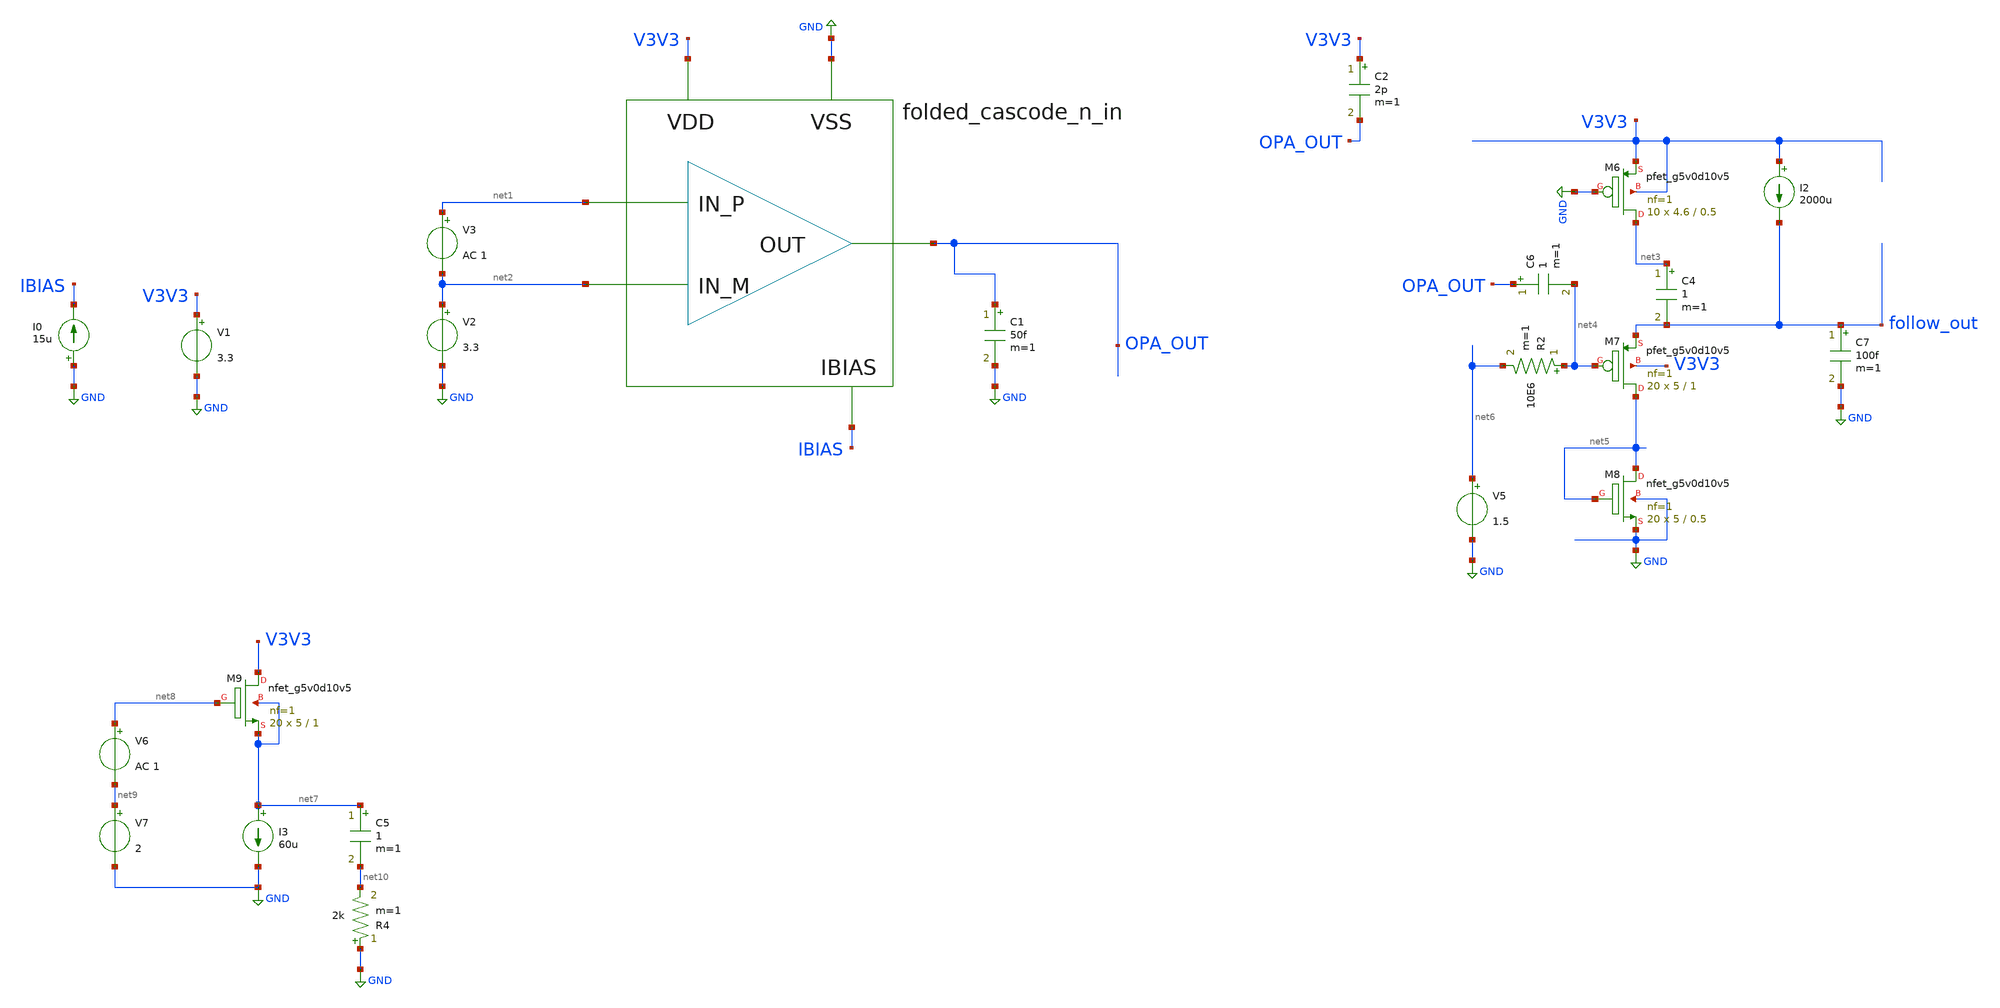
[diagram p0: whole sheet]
** sch_path: design/current-sense/current_sense_ac_bode.sch
**.subckt current_sense_ac_bode
V1 V3V3 GND 3.3
I0 GND IBIAS 15u
x1 net1 net2 OPA_OUT V3V3 GND IBIAS folded_cascode_n_in
C1 OPA_OUT GND 50f m=1
V2 net2 GND 3.3
V3 net1 net2 AC 1
XM6 net3 GND V3V3 V3V3 sky130_fd_pr__pfet_g5v0d10v5 L=0.5 W=4.6 nf=1 ad='int((nf+1)/2) * W/nf * 0.29'
+ as='int((nf+2)/2) * W/nf * 0.29' pd='2*int((nf+1)/2) * (W/nf + 0.29)' ps='2*int((nf+2)/2) * (W/nf + 0.29)'
+ nrd='0.29 / W' nrs='0.29 / W' sa=0 sb=0 sd=0 mult=10 m=10
XM7 net5 net4 follow_out V3V3 sky130_fd_pr__pfet_g5v0d10v5 L=1 W=5 nf=1 ad='int((nf+1)/2) * W/nf * 0.29'
+ as='int((nf+2)/2) * W/nf * 0.29' pd='2*int((nf+1)/2) * (W/nf + 0.29)' ps='2*int((nf+2)/2) * (W/nf + 0.29)'
+ nrd='0.29 / W' nrs='0.29 / W' sa=0 sb=0 sd=0 mult=20 m=20
I2 V3V3 follow_out 2000u
XM8 net5 net5 GND GND sky130_fd_pr__nfet_g5v0d10v5 L=0.5 W=5 nf=1 ad='int((nf+1)/2) * W/nf * 0.29' as='int((nf+2)/2) * W/nf * 0.29'
+ pd='2*int((nf+1)/2) * (W/nf + 0.29)' ps='2*int((nf+2)/2) * (W/nf + 0.29)' nrd='0.29 / W' nrs='0.29 / W'
+ sa=0 sb=0 sd=0 mult=20 m=20
V5 net6 GND 1.5
C4 net3 follow_out 1 m=1
XM9 V3V3 net8 net7 net7 sky130_fd_pr__nfet_g5v0d10v5 L=1 W=5 nf=1 ad='int((nf+1)/2) * W/nf * 0.29' as='int((nf+2)/2) * W/nf * 0.29'
+ pd='2*int((nf+1)/2) * (W/nf + 0.29)' ps='2*int((nf+2)/2) * (W/nf + 0.29)' nrd='0.29 / W' nrs='0.29 / W'
+ sa=0 sb=0 sd=0 mult=20 m=20
I3 net7 GND 60u
V6 net8 net9 AC 1
V7 net9 GND 2
R2 net4 net6 10E6 m=1
C5 net7 net10 1 m=1
R4 GND net10 2k m=1
C6 OPA_OUT net4 1 m=1
C7 follow_out GND 100f m=1
C2 V3V3 OPA_OUT 2p m=1
**** begin user architecture code



.control
.save all
.options savecurrents
ac dec 200 10 1000Meg
settype decibel opa_out
plot vdb(opa_out)
let opa_outd = 180/PI*cph(opa_out)
settype phase opa_outd
plot opa_outd

settype decibel follow_out
plot vdb(follow_out)
let follow_outd = 180/PI*cph(follow_out)
settype phase follow_outd
plot follow_outd
write current_sense_ac.raw
.endc



.lib $::SKYWATER_MODELS/models/sky130.lib.spice ss

**** end user architecture code
**.ends

* expanding   symbol:  design/folded-cascode-n-in/folded_cascode_n_in.sym # of pins=6
** sym_path: design/folded-cascode-n-in/folded_cascode_n_in.sym
** sch_path: design/folded-cascode-n-in/folded_cascode_n_in.sch
.subckt folded_cascode_n_in IN_P IN_M OUT VDD VSS VBN
*.ipin IN_P
*.ipin IN_M
*.ipin OUT
*.ipin VDD
*.ipin VSS
*.ipin VBN
XM1 net1 VBN VSS VSS sky130_fd_pr__nfet_g5v0d10v5 L=1 W=5 nf=1 ad='int((nf+1)/2) * W/nf * 0.29' as='int((nf+2)/2) * W/nf * 0.29'
+ pd='2*int((nf+1)/2) * (W/nf + 0.29)' ps='2*int((nf+2)/2) * (W/nf + 0.29)' nrd='0.29 / W' nrs='0.29 / W'
+ sa=0 sb=0 sd=0 mult=12 m=12
XM3 VS1_P IN_M net1 VSS sky130_fd_pr__nfet_g5v0d10v5 L=1 W=5 nf=1 ad='int((nf+1)/2) * W/nf * 0.29' as='int((nf+2)/2) * W/nf * 0.29'
+ pd='2*int((nf+1)/2) * (W/nf + 0.29)' ps='2*int((nf+2)/2) * (W/nf + 0.29)' nrd='0.29 / W' nrs='0.29 / W'
+ sa=0 sb=0 sd=0 mult=24 m=24
XM4 VS1_M IN_P net1 VSS sky130_fd_pr__nfet_g5v0d10v5 L=1 W=5 nf=1 ad='int((nf+1)/2) * W/nf * 0.29' as='int((nf+2)/2) * W/nf * 0.29'
+ pd='2*int((nf+1)/2) * (W/nf + 0.29)' ps='2*int((nf+2)/2) * (W/nf + 0.29)' nrd='0.29 / W' nrs='0.29 / W'
+ sa=0 sb=0 sd=0 mult=24 m=24
XM9 net2 VCN net4 VSS sky130_fd_pr__nfet_g5v0d10v5 L=1 W=5 nf=1 ad='int((nf+1)/2) * W/nf * 0.29' as='int((nf+2)/2) * W/nf * 0.29'
+ pd='2*int((nf+1)/2) * (W/nf + 0.29)' ps='2*int((nf+2)/2) * (W/nf + 0.29)' nrd='0.29 / W' nrs='0.29 / W'
+ sa=0 sb=0 sd=0 mult=4 m=4
XM10 net3 net2 VSS VSS sky130_fd_pr__nfet_g5v0d10v5 L=1 W=5 nf=1 ad='int((nf+1)/2) * W/nf * 0.29' as='int((nf+2)/2) * W/nf * 0.29'
+ pd='2*int((nf+1)/2) * (W/nf + 0.29)' ps='2*int((nf+2)/2) * (W/nf + 0.29)' nrd='0.29 / W' nrs='0.29 / W'
+ sa=0 sb=0 sd=0 mult=4 m=4
XM11 net4 net2 VSS VSS sky130_fd_pr__nfet_g5v0d10v5 L=1 W=5 nf=1 ad='int((nf+1)/2) * W/nf * 0.29' as='int((nf+2)/2) * W/nf * 0.29'
+ pd='2*int((nf+1)/2) * (W/nf + 0.29)' ps='2*int((nf+2)/2) * (W/nf + 0.29)' nrd='0.29 / W' nrs='0.29 / W'
+ sa=0 sb=0 sd=0 mult=4 m=4
XM12 OUT VCN net3 VSS sky130_fd_pr__nfet_g5v0d10v5 L=1 W=5 nf=1 ad='int((nf+1)/2) * W/nf * 0.29' as='int((nf+2)/2) * W/nf * 0.29'
+ pd='2*int((nf+1)/2) * (W/nf + 0.29)' ps='2*int((nf+2)/2) * (W/nf + 0.29)' nrd='0.29 / W' nrs='0.29 / W'
+ sa=0 sb=0 sd=0 mult=4 m=4
XM5 VS1_P VBP_INT VDD VDD sky130_fd_pr__pfet_g5v0d10v5 L=1 W=5 nf=1 ad='int((nf+1)/2) * W/nf * 0.29'
+ as='int((nf+2)/2) * W/nf * 0.29' pd='2*int((nf+1)/2) * (W/nf + 0.29)' ps='2*int((nf+2)/2) * (W/nf + 0.29)'
+ nrd='0.29 / W' nrs='0.29 / W' sa=0 sb=0 sd=0 mult=10 m=10
XM13 VS1_M VBP_INT VDD VDD sky130_fd_pr__pfet_g5v0d10v5 L=1 W=5 nf=1 ad='int((nf+1)/2) * W/nf * 0.29'
+ as='int((nf+2)/2) * W/nf * 0.29' pd='2*int((nf+1)/2) * (W/nf + 0.29)' ps='2*int((nf+2)/2) * (W/nf + 0.29)'
+ nrd='0.29 / W' nrs='0.29 / W' sa=0 sb=0 sd=0 mult=10 m=10
XM17 VBP_INT VBN VSS VSS sky130_fd_pr__nfet_g5v0d10v5 L=1 W=5 nf=1 ad='int((nf+1)/2) * W/nf * 0.29' as='int((nf+2)/2) * W/nf * 0.29'
+ pd='2*int((nf+1)/2) * (W/nf + 0.29)' ps='2*int((nf+2)/2) * (W/nf + 0.29)' nrd='0.29 / W' nrs='0.29 / W'
+ sa=0 sb=0 sd=0 mult=1 m=1
XM18 VBP_INT VBP_INT VDD VDD sky130_fd_pr__pfet_g5v0d10v5 L=1 W=5 nf=1 ad='int((nf+1)/2) * W/nf * 0.29'
+ as='int((nf+2)/2) * W/nf * 0.29' pd='2*int((nf+1)/2) * (W/nf + 0.29)' ps='2*int((nf+2)/2) * (W/nf + 0.29)'
+ nrd='0.29 / W' nrs='0.29 / W' sa=0 sb=0 sd=0 mult=1 m=1
XM14 net2 VCP VS1_M VDD sky130_fd_pr__pfet_g5v0d10v5 L=1 W=5 nf=1 ad='int((nf+1)/2) * W/nf * 0.29' as='int((nf+2)/2) * W/nf * 0.29'
+ pd='2*int((nf+1)/2) * (W/nf + 0.29)' ps='2*int((nf+2)/2) * (W/nf + 0.29)' nrd='0.29 / W' nrs='0.29 / W'
+ sa=0 sb=0 sd=0 mult=4 m=4
XM19 OUT VCP VS1_P VDD sky130_fd_pr__pfet_g5v0d10v5 L=1 W=5 nf=1 ad='int((nf+1)/2) * W/nf * 0.29' as='int((nf+2)/2) * W/nf * 0.29'
+ pd='2*int((nf+1)/2) * (W/nf + 0.29)' ps='2*int((nf+2)/2) * (W/nf + 0.29)' nrd='0.29 / W' nrs='0.29 / W'
+ sa=0 sb=0 sd=0 mult=4 m=4
XM2 VBP_INT VBP_INT VS1_P VSS sky130_fd_pr__nfet_g5v0d10v5 L=1 W=5 nf=1 ad='int((nf+1)/2) * W/nf * 0.29'
+ as='int((nf+2)/2) * W/nf * 0.29' pd='2*int((nf+1)/2) * (W/nf + 0.29)' ps='2*int((nf+2)/2) * (W/nf + 0.29)'
+ nrd='0.29 / W' nrs='0.29 / W' sa=0 sb=0 sd=0 mult=1 m=1
XM6 VBP_INT VBP_INT VS1_M VSS sky130_fd_pr__nfet_g5v0d10v5 L=1 W=5 nf=1 ad='int((nf+1)/2) * W/nf * 0.29'
+ as='int((nf+2)/2) * W/nf * 0.29' pd='2*int((nf+1)/2) * (W/nf + 0.29)' ps='2*int((nf+2)/2) * (W/nf + 0.29)'
+ nrd='0.29 / W' nrs='0.29 / W' sa=0 sb=0 sd=0 mult=1 m=1
x1 VBN VCN net5 VCP VDD VSS cascode_bias
.ends


* expanding   symbol:  design/bias-circuit/cascode_bias.sym # of pins=6
** sym_path: design/bias-circuit/cascode_bias.sym
** sch_path: design/bias-circuit/cascode_bias.sch
.subckt cascode_bias VBN VCN VBP VCP VDD VSS
*.ipin VCN
*.ipin VBP
*.ipin VCP
*.ipin VDD
*.ipin VSS
*.ipin VBN
XM1 VBP VBP VDD VDD sky130_fd_pr__pfet_g5v0d10v5 L=1 W=5 nf=1 ad='int((nf+1)/2) * W/nf * 0.29' as='int((nf+2)/2) * W/nf * 0.29'
+ pd='2*int((nf+1)/2) * (W/nf + 0.29)' ps='2*int((nf+2)/2) * (W/nf + 0.29)' nrd='0.29 / W' nrs='0.29 / W'
+ sa=0 sb=0 sd=0 mult=1 m=1
XM2 net1 VBP net8 VDD sky130_fd_pr__pfet_g5v0d10v5 L=1 W=5 nf=1 ad='int((nf+1)/2) * W/nf * 0.29' as='int((nf+2)/2) * W/nf * 0.29'
+ pd='2*int((nf+1)/2) * (W/nf + 0.29)' ps='2*int((nf+2)/2) * (W/nf + 0.29)' nrd='0.29 / W' nrs='0.29 / W'
+ sa=0 sb=0 sd=0 mult=1 m=1
XM3 VCN VBP VDD VDD sky130_fd_pr__pfet_g5v0d10v5 L=1 W=5 nf=1 ad='int((nf+1)/2) * W/nf * 0.29' as='int((nf+2)/2) * W/nf * 0.29'
+ pd='2*int((nf+1)/2) * (W/nf + 0.29)' ps='2*int((nf+2)/2) * (W/nf + 0.29)' nrd='0.29 / W' nrs='0.29 / W'
+ sa=0 sb=0 sd=0 mult=1 m=1
XM4 net1 net1 net2 VSS sky130_fd_pr__nfet_g5v0d10v5 L=1 W=5 nf=1 ad='int((nf+1)/2) * W/nf * 0.29' as='int((nf+2)/2) * W/nf * 0.29'
+ pd='2*int((nf+1)/2) * (W/nf + 0.29)' ps='2*int((nf+2)/2) * (W/nf + 0.29)' nrd='0.29 / W' nrs='0.29 / W'
+ sa=0 sb=0 sd=0 mult=2 m=2
XM5 net2 net1 VSS VSS sky130_fd_pr__nfet_g5v0d10v5 L=1 W=5 nf=1 ad='int((nf+1)/2) * W/nf * 0.29' as='int((nf+2)/2) * W/nf * 0.29'
+ pd='2*int((nf+1)/2) * (W/nf + 0.29)' ps='2*int((nf+2)/2) * (W/nf + 0.29)' nrd='0.29 / W' nrs='0.29 / W'
+ sa=0 sb=0 sd=0 mult=1 m=1
XM21 VCN VCN net2 VSS sky130_fd_pr__nfet_g5v0d10v5 L=1 W=5 nf=1 ad='int((nf+1)/2) * W/nf * 0.29' as='int((nf+2)/2) * W/nf * 0.29'
+ pd='2*int((nf+1)/2) * (W/nf + 0.29)' ps='2*int((nf+2)/2) * (W/nf + 0.29)' nrd='0.29 / W' nrs='0.29 / W'
+ sa=0 sb=0 sd=0 mult=1 m=1
XM6 net3 VBN net6 VSS sky130_fd_pr__nfet_g5v0d10v5 L=1 W=5 nf=1 ad='int((nf+1)/2) * W/nf * 0.29' as='int((nf+2)/2) * W/nf * 0.29'
+ pd='2*int((nf+1)/2) * (W/nf + 0.29)' ps='2*int((nf+2)/2) * (W/nf + 0.29)' nrd='0.29 / W' nrs='0.29 / W'
+ sa=0 sb=0 sd=0 mult=1 m=1
XM9 VCP VBN VSS VSS sky130_fd_pr__nfet_g5v0d10v5 L=1 W=5 nf=1 ad='int((nf+1)/2) * W/nf * 0.29' as='int((nf+2)/2) * W/nf * 0.29'
+ pd='2*int((nf+1)/2) * (W/nf + 0.29)' ps='2*int((nf+2)/2) * (W/nf + 0.29)' nrd='0.29 / W' nrs='0.29 / W'
+ sa=0 sb=0 sd=0 mult=1 m=1
XM10 net3 net3 net4 VDD sky130_fd_pr__pfet_g5v0d10v5 L=1 W=5 nf=1 ad='int((nf+1)/2) * W/nf * 0.29' as='int((nf+2)/2) * W/nf * 0.29'
+ pd='2*int((nf+1)/2) * (W/nf + 0.29)' ps='2*int((nf+2)/2) * (W/nf + 0.29)' nrd='0.29 / W' nrs='0.29 / W'
+ sa=0 sb=0 sd=0 mult=2 m=2
XM11 VCP VCP net4 VDD sky130_fd_pr__pfet_g5v0d10v5 L=1 W=5 nf=1 ad='int((nf+1)/2) * W/nf * 0.29' as='int((nf+2)/2) * W/nf * 0.29'
+ pd='2*int((nf+1)/2) * (W/nf + 0.29)' ps='2*int((nf+2)/2) * (W/nf + 0.29)' nrd='0.29 / W' nrs='0.29 / W'
+ sa=0 sb=0 sd=0 mult=1 m=1
XM28 net4 net3 VDD VDD sky130_fd_pr__pfet_g5v0d10v5 L=1 W=5 nf=1 ad='int((nf+1)/2) * W/nf * 0.29' as='int((nf+2)/2) * W/nf * 0.29'
+ pd='2*int((nf+1)/2) * (W/nf + 0.29)' ps='2*int((nf+2)/2) * (W/nf + 0.29)' nrd='0.29 / W' nrs='0.29 / W'
+ sa=0 sb=0 sd=0 mult=1 m=1
XM12 VBP VBN VSS VSS sky130_fd_pr__nfet_g5v0d10v5 L=1 W=5 nf=1 ad='int((nf+1)/2) * W/nf * 0.29' as='int((nf+2)/2) * W/nf * 0.29'
+ pd='2*int((nf+1)/2) * (W/nf + 0.29)' ps='2*int((nf+2)/2) * (W/nf + 0.29)' nrd='0.29 / W' nrs='0.29 / W'
+ sa=0 sb=0 sd=0 mult=1 m=1
XM32 net8 VBP net5 VDD sky130_fd_pr__pfet_g5v0d10v5 L=1 W=5 nf=1 ad='int((nf+1)/2) * W/nf * 0.29' as='int((nf+2)/2) * W/nf * 0.29'
+ pd='2*int((nf+1)/2) * (W/nf + 0.29)' ps='2*int((nf+2)/2) * (W/nf + 0.29)' nrd='0.29 / W' nrs='0.29 / W'
+ sa=0 sb=0 sd=0 mult=1 m=1
XM33 net5 VBP VDD VDD sky130_fd_pr__pfet_g5v0d10v5 L=1 W=5 nf=1 ad='int((nf+1)/2) * W/nf * 0.29' as='int((nf+2)/2) * W/nf * 0.29'
+ pd='2*int((nf+1)/2) * (W/nf + 0.29)' ps='2*int((nf+2)/2) * (W/nf + 0.29)' nrd='0.29 / W' nrs='0.29 / W'
+ sa=0 sb=0 sd=0 mult=1 m=1
XM34 net6 VBN net7 VSS sky130_fd_pr__nfet_g5v0d10v5 L=1 W=5 nf=1 ad='int((nf+1)/2) * W/nf * 0.29' as='int((nf+2)/2) * W/nf * 0.29'
+ pd='2*int((nf+1)/2) * (W/nf + 0.29)' ps='2*int((nf+2)/2) * (W/nf + 0.29)' nrd='0.29 / W' nrs='0.29 / W'
+ sa=0 sb=0 sd=0 mult=1 m=1
XM35 net7 VBN VSS VSS sky130_fd_pr__nfet_g5v0d10v5 L=1 W=5 nf=1 ad='int((nf+1)/2) * W/nf * 0.29' as='int((nf+2)/2) * W/nf * 0.29'
+ pd='2*int((nf+1)/2) * (W/nf + 0.29)' ps='2*int((nf+2)/2) * (W/nf + 0.29)' nrd='0.29 / W' nrs='0.29 / W'
+ sa=0 sb=0 sd=0 mult=1 m=1
XM13 VBN VBN VSS VSS sky130_fd_pr__nfet_g5v0d10v5 L=1 W=5 nf=1 ad='int((nf+1)/2) * W/nf * 0.29' as='int((nf+2)/2) * W/nf * 0.29'
+ pd='2*int((nf+1)/2) * (W/nf + 0.29)' ps='2*int((nf+2)/2) * (W/nf + 0.29)' nrd='0.29 / W' nrs='0.29 / W'
+ sa=0 sb=0 sd=0 mult=1 m=1
.ends

.GLOBAL GND
**** begin user architecture code
[sky130_models]
**** end user architecture code
.end
